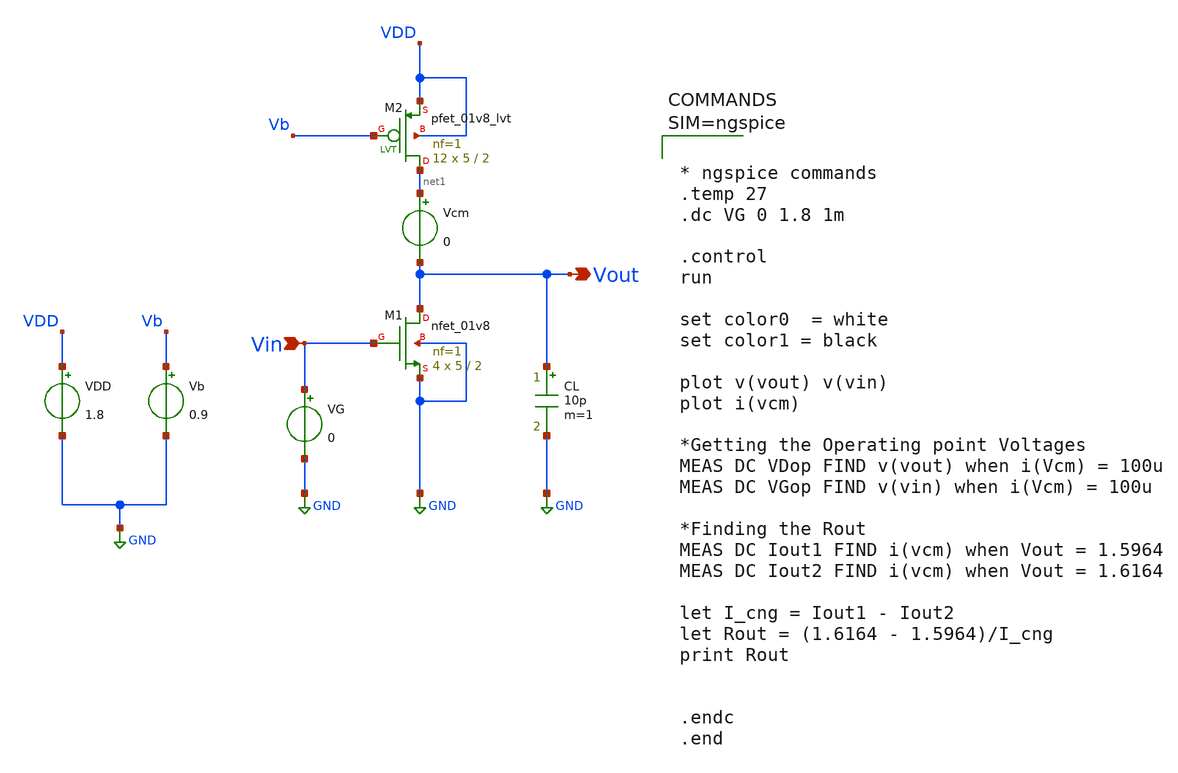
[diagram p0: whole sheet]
** sch_path: Common_Source_PMOS_Load_ckts/CS_Amp_PMOS_Sat_Load_Ckts/CS_Amp_PMOS_Sat_Load_DC_Analysis.sch
**.subckt CS_Amp_PMOS_Sat_Load_DC_Analysis Vin Vout
*.ipin Vin
*.opin Vout
XM1 Vout Vin GND GND sky130_fd_pr__nfet_01v8 L=2 W=5 nf=1 ad='int((1 + 1)/2) * 5 / 1 * 0.29' as='int((1 + 2)/2) * 5 / 1 * 0.29'
+ pd='2*int((1 + 1)/2) * (5 / 1 + 0.29)' ps='2*int((1 + 2)/2) * (5 / 1 + 0.29)' nrd='0.29 / 5 ' nrs='0.29 / 5 '
+ sa=0 sb=0 sd=0 mult=4 m=4
XM2 net1 Vb VDD VDD sky130_fd_pr__pfet_01v8_lvt L=2 W=5 nf=1 ad='int((1 + 1)/2) * 5 / 1 * 0.29' as='int((1 + 2)/2) * 5 / 1 * 0.29'
+ pd='2*int((1 + 1)/2) * (5 / 1 + 0.29)' ps='2*int((1 + 2)/2) * (5 / 1 + 0.29)' nrd='0.29 / 5 ' nrs='0.29 / 5 '
+ sa=0 sb=0 sd=0 mult=12 m=12
Vcm net1 Vout 0
VG Vin GND 0
Vb Vb GND 0.9
VDD VDD GND 1.8
CL Vout GND 10p m=1
**** begin user architecture code

** opencircuitdesign pdks install
.lib $::SKYWATER_MODELS/sky130.lib.spice tt




* ngspice commands
.temp 27
.dc VG 0 1.8 1m

.control
run

set color0  = white
set color1 = black

plot v(vout) v(vin)
plot i(vcm)

*Getting the Operating point Voltages
MEAS DC VDop FIND v(vout) when i(Vcm) = 100u
MEAS DC VGop FIND v(vin) when i(Vcm) = 100u

*Finding the Rout
MEAS DC Iout1 FIND i(vcm) when Vout = 1.5964
MEAS DC Iout2 FIND i(vcm) when Vout = 1.6164

let I_cng = Iout1 - Iout2
let Rout = (1.6164 - 1.5964)/I_cng
print Rout


.endc
.end




**** end user architecture code
**.ends
.GLOBAL GND
.end
